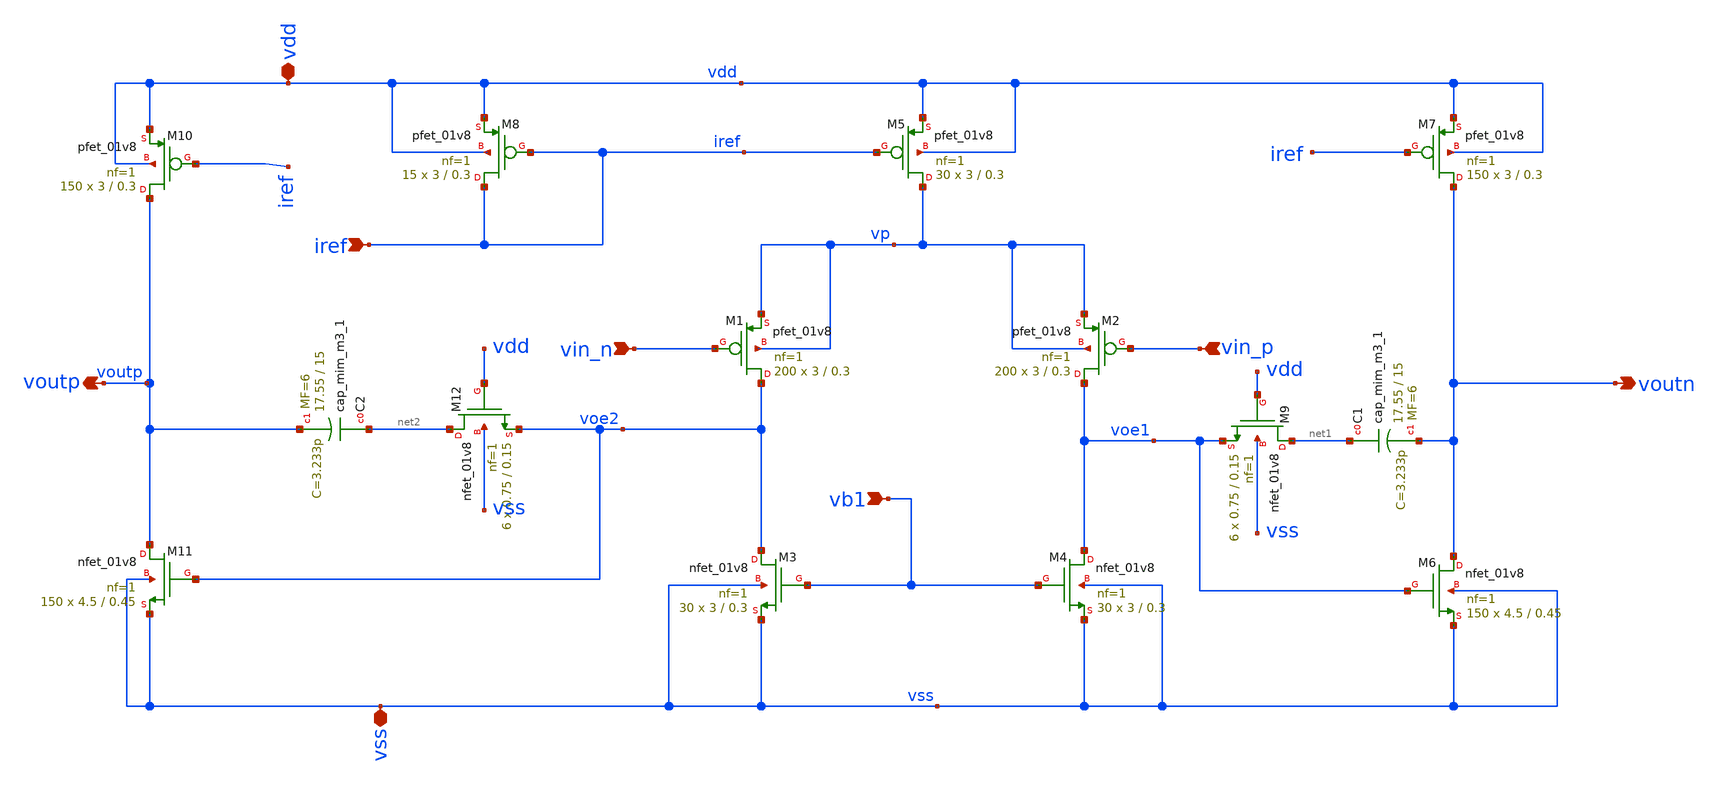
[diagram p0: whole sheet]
** sch_path: sch/opamp_sky130_dual.sch
**.subckt opamp_sky130_dual vdd vss vin_n vin_p iref voutn voutp vb1
*.iopin vdd
*.iopin vss
*.ipin vin_n
*.ipin vin_p
*.ipin iref
*.opin voutn
*.opin voutp
*.ipin vb1
XM1 voe2 vin_n vp vp sky130_fd_pr__pfet_01v8 L=0.3 W=3 nf=1 ad='W * 0.29' as='W * 0.29' pd='2 * (W + 0.29)'
+ ps='2 * (W + 0.29)' nrd='0.29 / W' nrs='0.29 / W' sa=0 sb=0 sd=0 mult=200 m=200
XM2 voe1 vin_p vp vp sky130_fd_pr__pfet_01v8 L=0.3 W=3 nf=1 ad='W * 0.29' as='W * 0.29' pd='2 * (W + 0.29)'
+ ps='2 * (W + 0.29)' nrd='0.29 / W' nrs='0.29 / W' sa=0 sb=0 sd=0 mult=200 m=200
XM3 voe2 vb1 vss vss sky130_fd_pr__nfet_01v8 L=0.3 W=3 nf=1 ad='W * 0.29' as='W * 0.29' pd='2 * (W + 0.29)'
+ ps='2 * (W + 0.29)' nrd='0.29 / W' nrs='0.29 / W' sa=0 sb=0 sd=0 mult=30 m=30
XM4 voe1 vb1 vss vss sky130_fd_pr__nfet_01v8 L=0.3 W=3 nf=1 ad='W * 0.29' as='W * 0.29' pd='2 * (W + 0.29)'
+ ps='2 * (W + 0.29)' nrd='0.29 / W' nrs='0.29 / W' sa=0 sb=0 sd=0 mult=30 m=30
XM5 vp iref vdd vdd sky130_fd_pr__pfet_01v8 L=0.3 W=3 nf=1 ad='W * 0.29' as='W * 0.29' pd='2 * (W + 0.29)'
+ ps='2 * (W + 0.29)' nrd='0.29 / W' nrs='0.29 / W' sa=0 sb=0 sd=0 mult=30 m=30
XM7 voutn iref vdd vdd sky130_fd_pr__pfet_01v8 L=0.3 W=3 nf=1 ad='W * 0.29' as='W * 0.29' pd='2 * (W + 0.29)'
+ ps='2 * (W + 0.29)' nrd='0.29 / W' nrs='0.29 / W' sa=0 sb=0 sd=0 mult=150 m=150
XM8 iref iref vdd vdd sky130_fd_pr__pfet_01v8 L=0.3 W=3 nf=1 ad='W * 0.29' as='W * 0.29' pd='2 * (W + 0.29)'
+ ps='2 * (W + 0.29)' nrd='0.29 / W' nrs='0.29 / W' sa=0 sb=0 sd=0 mult=15 m=15
XM9 net1 vdd voe1 vss sky130_fd_pr__nfet_01v8 L=0.15 W=0.75 nf=1 ad='W * 0.29' as='W * 0.29' pd='2 * (W + 0.29)'
+ ps='2 * (W + 0.29)' nrd='0.29 / W' nrs='0.29 / W' sa=0 sb=0 sd=0 mult=6 m=6
XC1 net1 voutn sky130_fd_pr__cap_mim_m3_1 W=17.55 L=15 MF=6 m=6
XM6 voutn voe1 vss vss sky130_fd_pr__nfet_01v8 L=0.45 W=4.5 nf=1 ad='W * 0.29' as='W * 0.29' pd='2 * (W + 0.29)'
+ ps='2 * (W + 0.29)' nrd='0.29 / W' nrs='0.29 / W' sa=0 sb=0 sd=0 mult=150 m=150
XM10 voutp iref vdd vdd sky130_fd_pr__pfet_01v8 L=0.3 W=3 nf=1 ad='W * 0.29' as='W * 0.29' pd='2 * (W + 0.29)'
+ ps='2 * (W + 0.29)' nrd='0.29 / W' nrs='0.29 / W' sa=0 sb=0 sd=0 mult=150 m=150
XM11 voutp voe2 vss vss sky130_fd_pr__nfet_01v8 L=0.45 W=4.5 nf=1 ad='W * 0.29' as='W * 0.29' pd='2 * (W + 0.29)'
+ ps='2 * (W + 0.29)' nrd='0.29 / W' nrs='0.29 / W' sa=0 sb=0 sd=0 mult=150 m=150
XM12 net2 vdd voe2 vss sky130_fd_pr__nfet_01v8 L=0.15 W=0.75 nf=1 ad='W * 0.29' as='W * 0.29' pd='2 * (W + 0.29)'
+ ps='2 * (W + 0.29)' nrd='0.29 / W' nrs='0.29 / W' sa=0 sb=0 sd=0 mult=6 m=6
XC2 net2 voutp sky130_fd_pr__cap_mim_m3_1 W=17.55 L=15 MF=6 m=6
**.ends
.end
